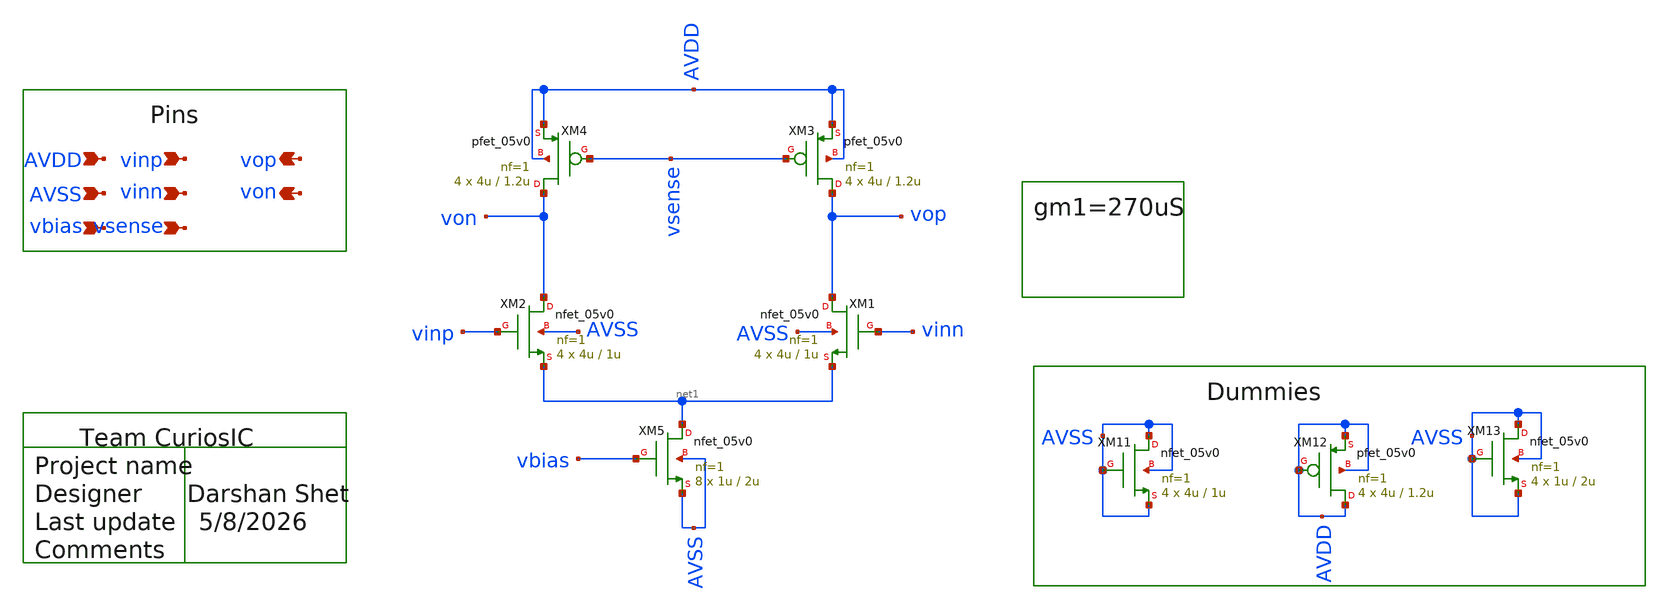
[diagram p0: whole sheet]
** sch_path: design/schematics/ADC/DSM_Loop_filter/First_int/OTA_Files/DS_cic_bms_afe_iadc_first_int_OTA_gm1.sch
**.subckt DS_cic_bms_afe_iadc_first_int_OTA_gm1 vinp vinn von vop AVDD AVSS vsense vbias
*.ipin vinp
*.ipin vinn
*.opin von
*.opin vop
*.ipin AVDD
*.ipin AVSS
*.ipin vsense
*.ipin vbias
XM1 vop vinn net1 AVSS nfet_05v0 L=1u W=4u nf=1 ad='int((nf+1)/2) * W/nf * 0.18u' as='int((nf+2)/2) * W/nf * 0.18u'
+ pd='2*int((nf+1)/2) * (W/nf + 0.18u)' ps='2*int((nf+2)/2) * (W/nf + 0.18u)' nrd='0.18u / W' nrs='0.18u / W'
+ sa=0 sb=0 sd=0 m=4
XM2 von vinp net1 AVSS nfet_05v0 L=1u W=4u nf=1 ad='int((nf+1)/2) * W/nf * 0.18u' as='int((nf+2)/2) * W/nf * 0.18u'
+ pd='2*int((nf+1)/2) * (W/nf + 0.18u)' ps='2*int((nf+2)/2) * (W/nf + 0.18u)' nrd='0.18u / W' nrs='0.18u / W'
+ sa=0 sb=0 sd=0 m=4
XM3 vop vsense AVDD AVDD pfet_05v0 L=1.2u W=4u nf=1 ad='int((nf+1)/2) * W/nf * 0.18u' as='int((nf+2)/2) * W/nf * 0.18u'
+ pd='2*int((nf+1)/2) * (W/nf + 0.18u)' ps='2*int((nf+2)/2) * (W/nf + 0.18u)' nrd='0.18u / W' nrs='0.18u / W'
+ sa=0 sb=0 sd=0 m=4
XM4 von vsense AVDD AVDD pfet_05v0 L=1.2u W=4u nf=1 ad='int((nf+1)/2) * W/nf * 0.18u' as='int((nf+2)/2) * W/nf * 0.18u'
+ pd='2*int((nf+1)/2) * (W/nf + 0.18u)' ps='2*int((nf+2)/2) * (W/nf + 0.18u)' nrd='0.18u / W' nrs='0.18u / W'
+ sa=0 sb=0 sd=0 m=4
XM5 net1 vbias AVSS AVSS nfet_05v0 L=2u W=1u nf=1 ad='int((nf+1)/2) * W/nf * 0.18u' as='int((nf+2)/2) * W/nf * 0.18u'
+ pd='2*int((nf+1)/2) * (W/nf + 0.18u)' ps='2*int((nf+2)/2) * (W/nf + 0.18u)' nrd='0.18u / W' nrs='0.18u / W'
+ sa=0 sb=0 sd=0 m=8
XM11 AVSS AVSS AVSS AVSS nfet_05v0 L=1u W=4u nf=1 ad='int((nf+1)/2) * W/nf * 0.18u' as='int((nf+2)/2) * W/nf * 0.18u'
+ pd='2*int((nf+1)/2) * (W/nf + 0.18u)' ps='2*int((nf+2)/2) * (W/nf + 0.18u)' nrd='0.18u / W' nrs='0.18u / W'
+ sa=0 sb=0 sd=0 m=4
XM12 AVDD AVDD AVDD AVDD pfet_05v0 L=1.2u W=4u nf=1 ad='int((nf+1)/2) * W/nf * 0.18u' as='int((nf+2)/2) * W/nf * 0.18u'
+ pd='2*int((nf+1)/2) * (W/nf + 0.18u)' ps='2*int((nf+2)/2) * (W/nf + 0.18u)' nrd='0.18u / W' nrs='0.18u / W'
+ sa=0 sb=0 sd=0 m=4
XM13 AVSS AVSS AVSS AVSS nfet_05v0 L=2u W=1u nf=1 ad='int((nf+1)/2) * W/nf * 0.18u' as='int((nf+2)/2) * W/nf * 0.18u'
+ pd='2*int((nf+1)/2) * (W/nf + 0.18u)' ps='2*int((nf+2)/2) * (W/nf + 0.18u)' nrd='0.18u / W' nrs='0.18u / W'
+ sa=0 sb=0 sd=0 m=4
**.ends
.end
